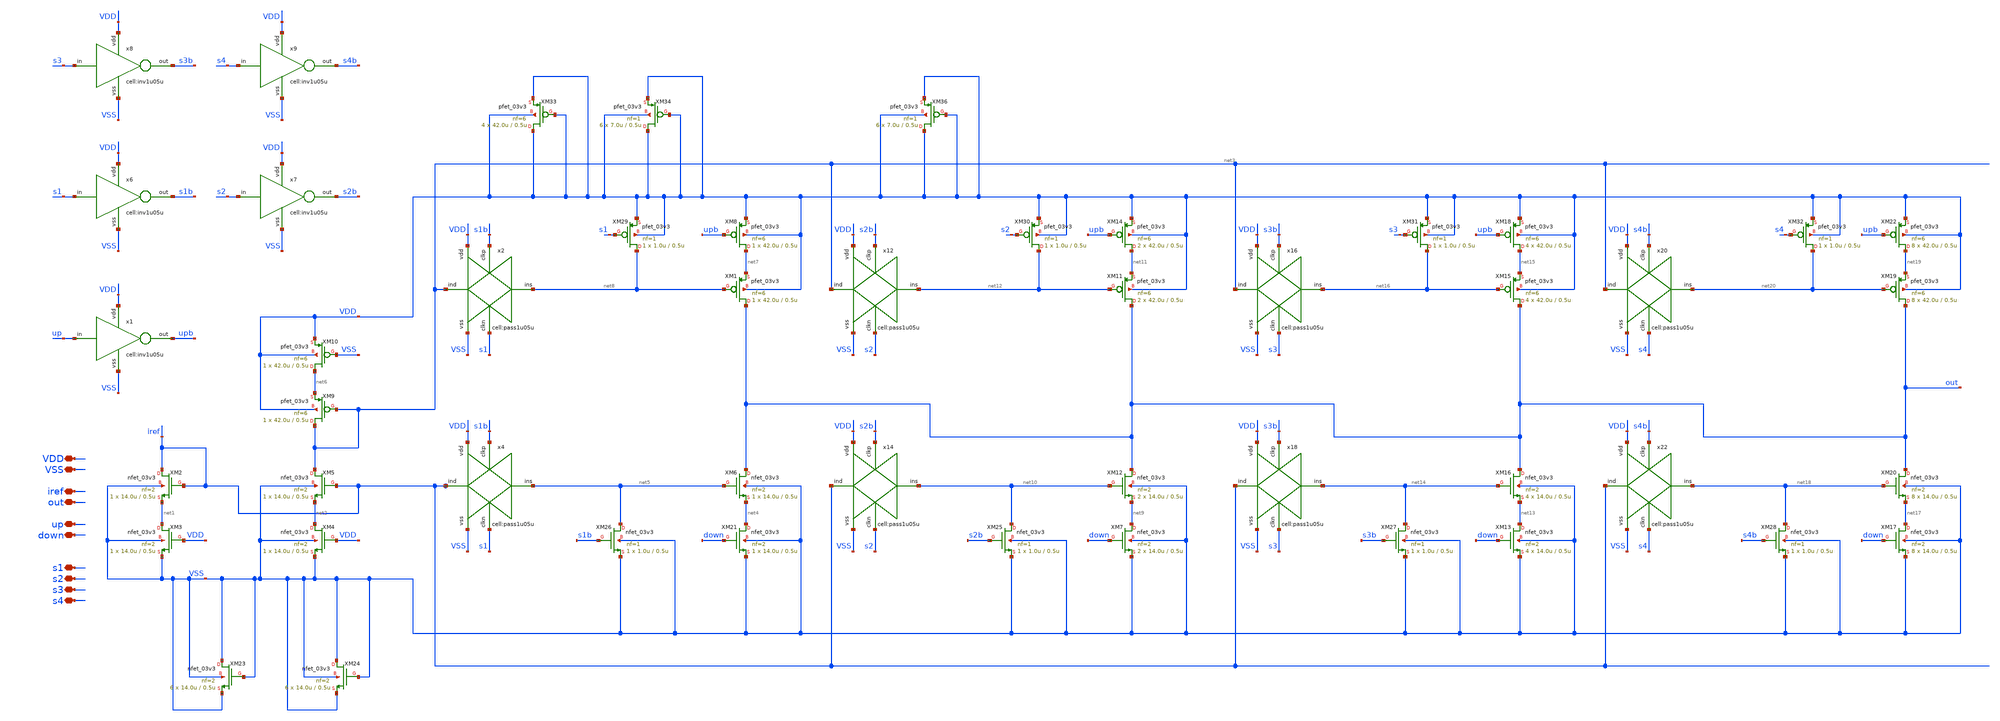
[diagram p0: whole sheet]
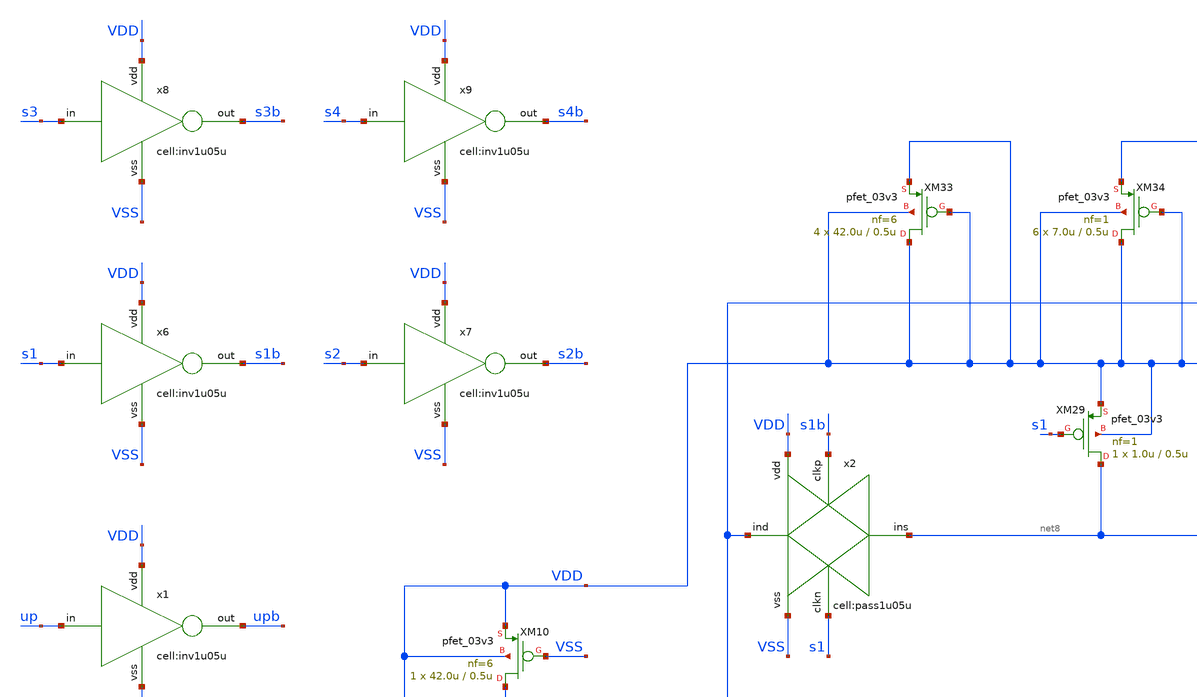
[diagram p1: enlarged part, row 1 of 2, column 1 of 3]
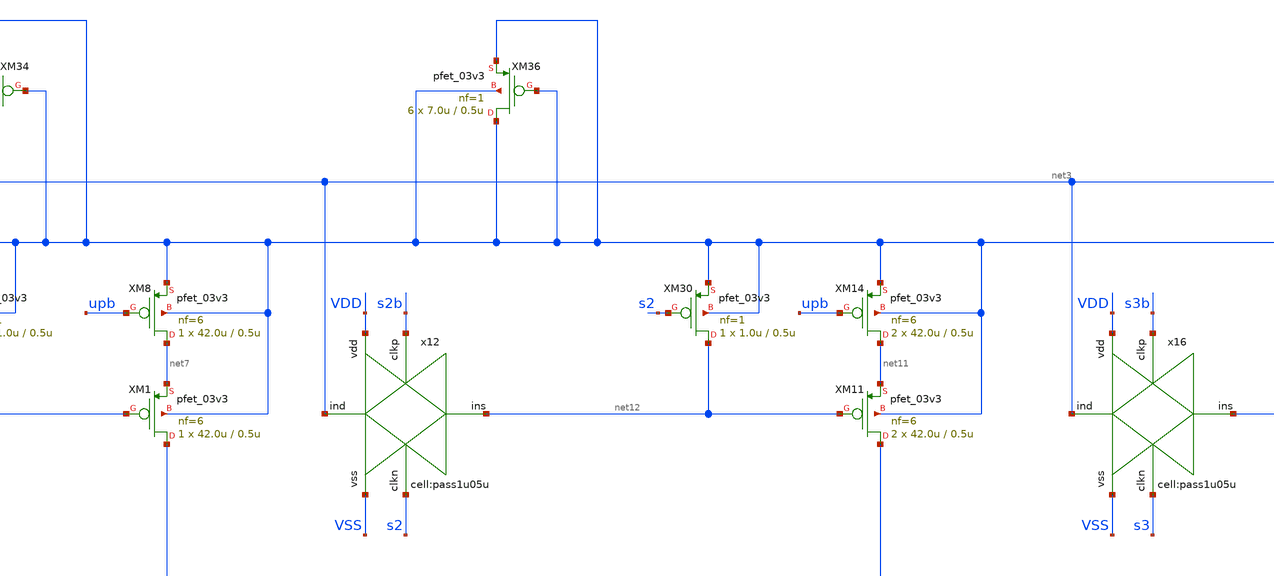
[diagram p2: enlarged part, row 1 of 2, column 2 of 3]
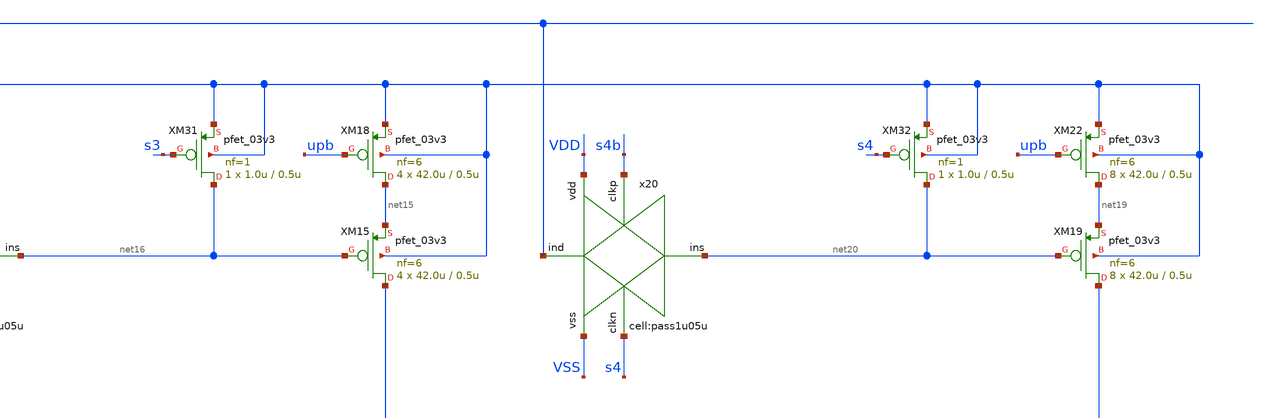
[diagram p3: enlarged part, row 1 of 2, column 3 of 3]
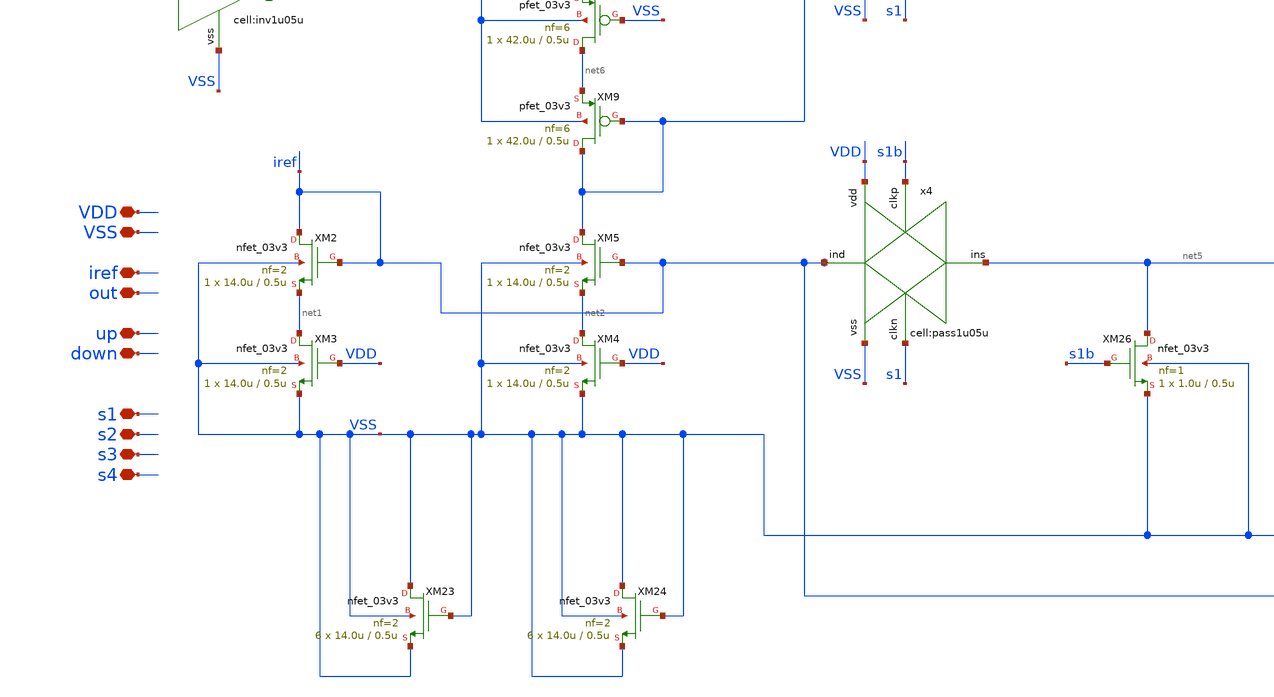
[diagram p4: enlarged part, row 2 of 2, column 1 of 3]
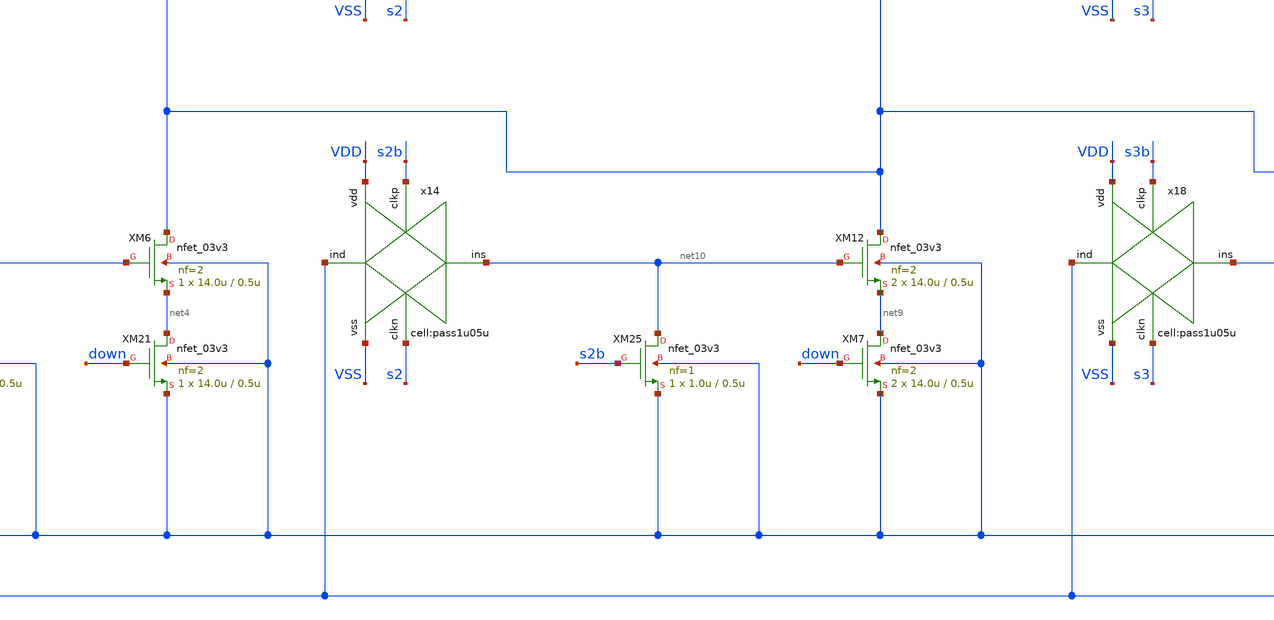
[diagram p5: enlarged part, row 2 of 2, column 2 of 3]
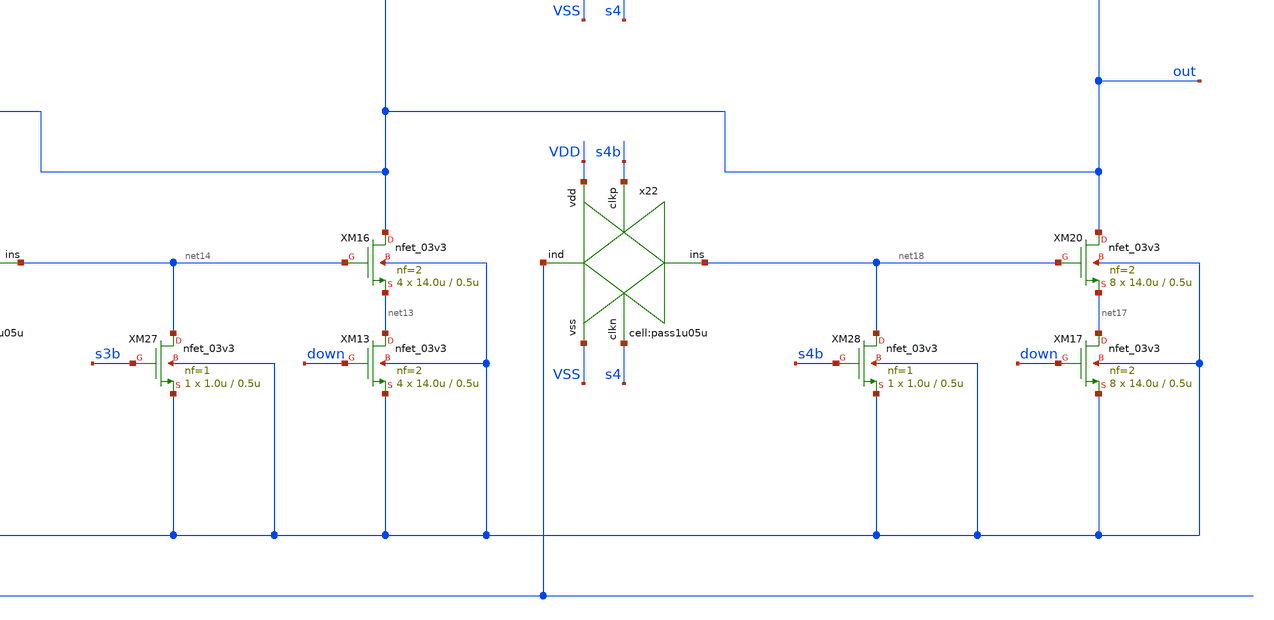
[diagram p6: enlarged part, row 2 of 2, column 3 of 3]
** sch_path: designs/libs/xp_core_analog/xp_programmable_basic_pump_flatten/xp_programmable_basic_pump.sch
**.subckt xp_programmable_basic_pump VDD VSS up down iref out s3 s4 s1 s2
*.iopin VDD
*.iopin VSS
*.iopin up
*.iopin down
*.iopin iref
*.iopin out
*.iopin s3
*.iopin s4
*.iopin s1
*.iopin s2
XM6 out net5 net4 VSS nfet_03v3 L=0.5u W=14.0u nf=2 ad='int((nf+1)/2) * W/nf * 0.18u' as='int((nf+2)/2) * W/nf * 0.18u'
+ pd='2*int((nf+1)/2) * (W/nf + 0.18u)' ps='2*int((nf+2)/2) * (W/nf + 0.18u)' nrd='0.18u / W' nrs='0.18u / W'
+ sa=0 sb=0 sd=0 m=1
XM8 net7 upb VDD VDD pfet_03v3 L=0.5u W=42.0u nf=6 ad='int((nf+1)/2) * W/nf * 0.18u' as='int((nf+2)/2) * W/nf * 0.18u'
+ pd='2*int((nf+1)/2) * (W/nf + 0.18u)' ps='2*int((nf+2)/2) * (W/nf + 0.18u)' nrd='0.18u / W' nrs='0.18u / W'
+ sa=0 sb=0 sd=0 m=1
XM10 net6 VSS VDD VDD pfet_03v3 L=0.5u W=42.0u nf=6 ad='int((nf+1)/2) * W/nf * 0.18u' as='int((nf+2)/2) * W/nf * 0.18u'
+ pd='2*int((nf+1)/2) * (W/nf + 0.18u)' ps='2*int((nf+2)/2) * (W/nf + 0.18u)' nrd='0.18u / W' nrs='0.18u / W'
+ sa=0 sb=0 sd=0 m=1
x1 up VDD upb VSS inv1u05u
x2 net3 VSS s1 net8 s1b VDD pass1u05u
x4 iref VSS s1 net5 s1b VDD pass1u05u
x6 s1 VDD s1b VSS inv1u05u
x7 s2 VDD s2b VSS inv1u05u
x8 s3 VDD s3b VSS inv1u05u
x9 s4 VDD s4b VSS inv1u05u
XM12 out net10 net9 VSS nfet_03v3 L=0.5u W=14.0u nf=2 ad='int((nf+1)/2) * W/nf * 0.18u' as='int((nf+2)/2) * W/nf * 0.18u'
+ pd='2*int((nf+1)/2) * (W/nf + 0.18u)' ps='2*int((nf+2)/2) * (W/nf + 0.18u)' nrd='0.18u / W' nrs='0.18u / W'
+ sa=0 sb=0 sd=0 m=2
XM14 net11 upb VDD VDD pfet_03v3 L=0.5u W=42.0u nf=6 ad='int((nf+1)/2) * W/nf * 0.18u' as='int((nf+2)/2) * W/nf * 0.18u'
+ pd='2*int((nf+1)/2) * (W/nf + 0.18u)' ps='2*int((nf+2)/2) * (W/nf + 0.18u)' nrd='0.18u / W' nrs='0.18u / W'
+ sa=0 sb=0 sd=0 m=2
x12 net3 VSS s2 net12 s2b VDD pass1u05u
x14 iref VSS s2 net10 s2b VDD pass1u05u
XM16 out net14 net13 VSS nfet_03v3 L=0.5u W=14.0u nf=2 ad='int((nf+1)/2) * W/nf * 0.18u' as='int((nf+2)/2) * W/nf * 0.18u'
+ pd='2*int((nf+1)/2) * (W/nf + 0.18u)' ps='2*int((nf+2)/2) * (W/nf + 0.18u)' nrd='0.18u / W' nrs='0.18u / W'
+ sa=0 sb=0 sd=0 m=4
XM18 net15 upb VDD VDD pfet_03v3 L=0.5u W=42.0u nf=6 ad='int((nf+1)/2) * W/nf * 0.18u' as='int((nf+2)/2) * W/nf * 0.18u'
+ pd='2*int((nf+1)/2) * (W/nf + 0.18u)' ps='2*int((nf+2)/2) * (W/nf + 0.18u)' nrd='0.18u / W' nrs='0.18u / W'
+ sa=0 sb=0 sd=0 m=4
x16 net3 VSS s3 net16 s3b VDD pass1u05u
x18 iref VSS s3 net14 s3b VDD pass1u05u
XM19 out net20 net19 VDD pfet_03v3 L=0.5u W=42.0u nf=6 ad='int((nf+1)/2) * W/nf * 0.18u' as='int((nf+2)/2) * W/nf * 0.18u'
+ pd='2*int((nf+1)/2) * (W/nf + 0.18u)' ps='2*int((nf+2)/2) * (W/nf + 0.18u)' nrd='0.18u / W' nrs='0.18u / W'
+ sa=0 sb=0 sd=0 m=8
XM20 out net18 net17 VSS nfet_03v3 L=0.5u W=14.0u nf=2 ad='int((nf+1)/2) * W/nf * 0.18u' as='int((nf+2)/2) * W/nf * 0.18u'
+ pd='2*int((nf+1)/2) * (W/nf + 0.18u)' ps='2*int((nf+2)/2) * (W/nf + 0.18u)' nrd='0.18u / W' nrs='0.18u / W'
+ sa=0 sb=0 sd=0 m=8
XM22 net19 upb VDD VDD pfet_03v3 L=0.5u W=42.0u nf=6 ad='int((nf+1)/2) * W/nf * 0.18u' as='int((nf+2)/2) * W/nf * 0.18u'
+ pd='2*int((nf+1)/2) * (W/nf + 0.18u)' ps='2*int((nf+2)/2) * (W/nf + 0.18u)' nrd='0.18u / W' nrs='0.18u / W'
+ sa=0 sb=0 sd=0 m=8
x20 net3 VSS s4 net20 s4b VDD pass1u05u
x22 iref VSS s4 net18 s4b VDD pass1u05u
XM2 iref iref net1 VSS nfet_03v3 L=0.5u W=14.0u nf=2 ad='int((nf+1)/2) * W/nf * 0.18u' as='int((nf+2)/2) * W/nf * 0.18u'
+ pd='2*int((nf+1)/2) * (W/nf + 0.18u)' ps='2*int((nf+2)/2) * (W/nf + 0.18u)' nrd='0.18u / W' nrs='0.18u / W'
+ sa=0 sb=0 sd=0 m=1
XM9 net3 net3 net6 VDD pfet_03v3 L=0.5u W=42.0u nf=6 ad='int((nf+1)/2) * W/nf * 0.18u' as='int((nf+2)/2) * W/nf * 0.18u'
+ pd='2*int((nf+1)/2) * (W/nf + 0.18u)' ps='2*int((nf+2)/2) * (W/nf + 0.18u)' nrd='0.18u / W' nrs='0.18u / W'
+ sa=0 sb=0 sd=0 m=1
XM1 out net8 net7 VDD pfet_03v3 L=0.5u W=42.0u nf=6 ad='int((nf+1)/2) * W/nf * 0.18u' as='int((nf+2)/2) * W/nf * 0.18u'
+ pd='2*int((nf+1)/2) * (W/nf + 0.18u)' ps='2*int((nf+2)/2) * (W/nf + 0.18u)' nrd='0.18u / W' nrs='0.18u / W'
+ sa=0 sb=0 sd=0 m=1
XM11 out net12 net11 VDD pfet_03v3 L=0.5u W=42.0u nf=6 ad='int((nf+1)/2) * W/nf * 0.18u' as='int((nf+2)/2) * W/nf * 0.18u'
+ pd='2*int((nf+1)/2) * (W/nf + 0.18u)' ps='2*int((nf+2)/2) * (W/nf + 0.18u)' nrd='0.18u / W' nrs='0.18u / W'
+ sa=0 sb=0 sd=0 m=2
XM15 out net16 net15 VDD pfet_03v3 L=0.5u W=42.0u nf=6 ad='int((nf+1)/2) * W/nf * 0.18u' as='int((nf+2)/2) * W/nf * 0.18u'
+ pd='2*int((nf+1)/2) * (W/nf + 0.18u)' ps='2*int((nf+2)/2) * (W/nf + 0.18u)' nrd='0.18u / W' nrs='0.18u / W'
+ sa=0 sb=0 sd=0 m=4
XM3 net1 VDD VSS VSS nfet_03v3 L=0.5u W=14.0u nf=2 ad='int((nf+1)/2) * W/nf * 0.18u' as='int((nf+2)/2) * W/nf * 0.18u'
+ pd='2*int((nf+1)/2) * (W/nf + 0.18u)' ps='2*int((nf+2)/2) * (W/nf + 0.18u)' nrd='0.18u / W' nrs='0.18u / W'
+ sa=0 sb=0 sd=0 m=1
XM4 net2 VDD VSS VSS nfet_03v3 L=0.5u W=14.0u nf=2 ad='int((nf+1)/2) * W/nf * 0.18u' as='int((nf+2)/2) * W/nf * 0.18u'
+ pd='2*int((nf+1)/2) * (W/nf + 0.18u)' ps='2*int((nf+2)/2) * (W/nf + 0.18u)' nrd='0.18u / W' nrs='0.18u / W'
+ sa=0 sb=0 sd=0 m=1
XM5 net3 iref net2 VSS nfet_03v3 L=0.5u W=14.0u nf=2 ad='int((nf+1)/2) * W/nf * 0.18u' as='int((nf+2)/2) * W/nf * 0.18u'
+ pd='2*int((nf+1)/2) * (W/nf + 0.18u)' ps='2*int((nf+2)/2) * (W/nf + 0.18u)' nrd='0.18u / W' nrs='0.18u / W'
+ sa=0 sb=0 sd=0 m=1
XM21 net4 down VSS VSS nfet_03v3 L=0.5u W=14.0u nf=2 ad='int((nf+1)/2) * W/nf * 0.18u' as='int((nf+2)/2) * W/nf * 0.18u'
+ pd='2*int((nf+1)/2) * (W/nf + 0.18u)' ps='2*int((nf+2)/2) * (W/nf + 0.18u)' nrd='0.18u / W' nrs='0.18u / W'
+ sa=0 sb=0 sd=0 m=1
XM7 net9 down VSS VSS nfet_03v3 L=0.5u W=14.0u nf=2 ad='int((nf+1)/2) * W/nf * 0.18u' as='int((nf+2)/2) * W/nf * 0.18u'
+ pd='2*int((nf+1)/2) * (W/nf + 0.18u)' ps='2*int((nf+2)/2) * (W/nf + 0.18u)' nrd='0.18u / W' nrs='0.18u / W'
+ sa=0 sb=0 sd=0 m=2
XM13 net13 down VSS VSS nfet_03v3 L=0.5u W=14.0u nf=2 ad='int((nf+1)/2) * W/nf * 0.18u' as='int((nf+2)/2) * W/nf * 0.18u'
+ pd='2*int((nf+1)/2) * (W/nf + 0.18u)' ps='2*int((nf+2)/2) * (W/nf + 0.18u)' nrd='0.18u / W' nrs='0.18u / W'
+ sa=0 sb=0 sd=0 m=4
XM17 net17 down VSS VSS nfet_03v3 L=0.5u W=14.0u nf=2 ad='int((nf+1)/2) * W/nf * 0.18u' as='int((nf+2)/2) * W/nf * 0.18u'
+ pd='2*int((nf+1)/2) * (W/nf + 0.18u)' ps='2*int((nf+2)/2) * (W/nf + 0.18u)' nrd='0.18u / W' nrs='0.18u / W'
+ sa=0 sb=0 sd=0 m=8
XM23 VSS VSS VSS VSS nfet_03v3 L=0.5u W=14.0u nf=2 ad='int((nf+1)/2) * W/nf * 0.18u' as='int((nf+2)/2) * W/nf * 0.18u'
+ pd='2*int((nf+1)/2) * (W/nf + 0.18u)' ps='2*int((nf+2)/2) * (W/nf + 0.18u)' nrd='0.18u / W' nrs='0.18u / W'
+ sa=0 sb=0 sd=0 m=6
XM24 VSS VSS VSS VSS nfet_03v3 L=0.5u W=14.0u nf=2 ad='int((nf+1)/2) * W/nf * 0.18u' as='int((nf+2)/2) * W/nf * 0.18u'
+ pd='2*int((nf+1)/2) * (W/nf + 0.18u)' ps='2*int((nf+2)/2) * (W/nf + 0.18u)' nrd='0.18u / W' nrs='0.18u / W'
+ sa=0 sb=0 sd=0 m=6
XM26 net5 s1b VSS VSS nfet_03v3 L=0.5u W=1.0u nf=1 ad='int((nf+1)/2) * W/nf * 0.18u' as='int((nf+2)/2) * W/nf * 0.18u'
+ pd='2*int((nf+1)/2) * (W/nf + 0.18u)' ps='2*int((nf+2)/2) * (W/nf + 0.18u)' nrd='0.18u / W' nrs='0.18u / W'
+ sa=0 sb=0 sd=0 m=1
XM29 net8 s1 VDD VDD pfet_03v3 L=0.5u W=1.0u nf=1 ad='int((nf+1)/2) * W/nf * 0.18u' as='int((nf+2)/2) * W/nf * 0.18u'
+ pd='2*int((nf+1)/2) * (W/nf + 0.18u)' ps='2*int((nf+2)/2) * (W/nf + 0.18u)' nrd='0.18u / W' nrs='0.18u / W'
+ sa=0 sb=0 sd=0 m=1
XM33 VDD VDD VDD VDD pfet_03v3 L=0.5u W=42.0u nf=6 ad='int((nf+1)/2) * W/nf * 0.18u' as='int((nf+2)/2) * W/nf * 0.18u'
+ pd='2*int((nf+1)/2) * (W/nf + 0.18u)' ps='2*int((nf+2)/2) * (W/nf + 0.18u)' nrd='0.18u / W' nrs='0.18u / W'
+ sa=0 sb=0 sd=0 m=4
XM34 VDD VDD VDD VDD pfet_03v3 L=0.5u W=7.0u nf=1 ad='int((nf+1)/2) * W/nf * 0.18u' as='int((nf+2)/2) * W/nf * 0.18u'
+ pd='2*int((nf+1)/2) * (W/nf + 0.18u)' ps='2*int((nf+2)/2) * (W/nf + 0.18u)' nrd='0.18u / W' nrs='0.18u / W'
+ sa=0 sb=0 sd=0 m=6
XM36 VDD VDD VDD VDD pfet_03v3 L=0.5u W=7.0u nf=1 ad='int((nf+1)/2) * W/nf * 0.18u' as='int((nf+2)/2) * W/nf * 0.18u'
+ pd='2*int((nf+1)/2) * (W/nf + 0.18u)' ps='2*int((nf+2)/2) * (W/nf + 0.18u)' nrd='0.18u / W' nrs='0.18u / W'
+ sa=0 sb=0 sd=0 m=6
XM25 net10 s2b VSS VSS nfet_03v3 L=0.5u W=1.0u nf=1 ad='int((nf+1)/2) * W/nf * 0.18u' as='int((nf+2)/2) * W/nf * 0.18u'
+ pd='2*int((nf+1)/2) * (W/nf + 0.18u)' ps='2*int((nf+2)/2) * (W/nf + 0.18u)' nrd='0.18u / W' nrs='0.18u / W'
+ sa=0 sb=0 sd=0 m=1
XM27 net14 s3b VSS VSS nfet_03v3 L=0.5u W=1.0u nf=1 ad='int((nf+1)/2) * W/nf * 0.18u' as='int((nf+2)/2) * W/nf * 0.18u'
+ pd='2*int((nf+1)/2) * (W/nf + 0.18u)' ps='2*int((nf+2)/2) * (W/nf + 0.18u)' nrd='0.18u / W' nrs='0.18u / W'
+ sa=0 sb=0 sd=0 m=1
XM28 net18 s4b VSS VSS nfet_03v3 L=0.5u W=1.0u nf=1 ad='int((nf+1)/2) * W/nf * 0.18u' as='int((nf+2)/2) * W/nf * 0.18u'
+ pd='2*int((nf+1)/2) * (W/nf + 0.18u)' ps='2*int((nf+2)/2) * (W/nf + 0.18u)' nrd='0.18u / W' nrs='0.18u / W'
+ sa=0 sb=0 sd=0 m=1
XM30 net12 s2 VDD VDD pfet_03v3 L=0.5u W=1.0u nf=1 ad='int((nf+1)/2) * W/nf * 0.18u' as='int((nf+2)/2) * W/nf * 0.18u'
+ pd='2*int((nf+1)/2) * (W/nf + 0.18u)' ps='2*int((nf+2)/2) * (W/nf + 0.18u)' nrd='0.18u / W' nrs='0.18u / W'
+ sa=0 sb=0 sd=0 m=1
XM31 net16 s3 VDD VDD pfet_03v3 L=0.5u W=1.0u nf=1 ad='int((nf+1)/2) * W/nf * 0.18u' as='int((nf+2)/2) * W/nf * 0.18u'
+ pd='2*int((nf+1)/2) * (W/nf + 0.18u)' ps='2*int((nf+2)/2) * (W/nf + 0.18u)' nrd='0.18u / W' nrs='0.18u / W'
+ sa=0 sb=0 sd=0 m=1
XM32 net20 s4 VDD VDD pfet_03v3 L=0.5u W=1.0u nf=1 ad='int((nf+1)/2) * W/nf * 0.18u' as='int((nf+2)/2) * W/nf * 0.18u'
+ pd='2*int((nf+1)/2) * (W/nf + 0.18u)' ps='2*int((nf+2)/2) * (W/nf + 0.18u)' nrd='0.18u / W' nrs='0.18u / W'
+ sa=0 sb=0 sd=0 m=1
**.ends
.end
